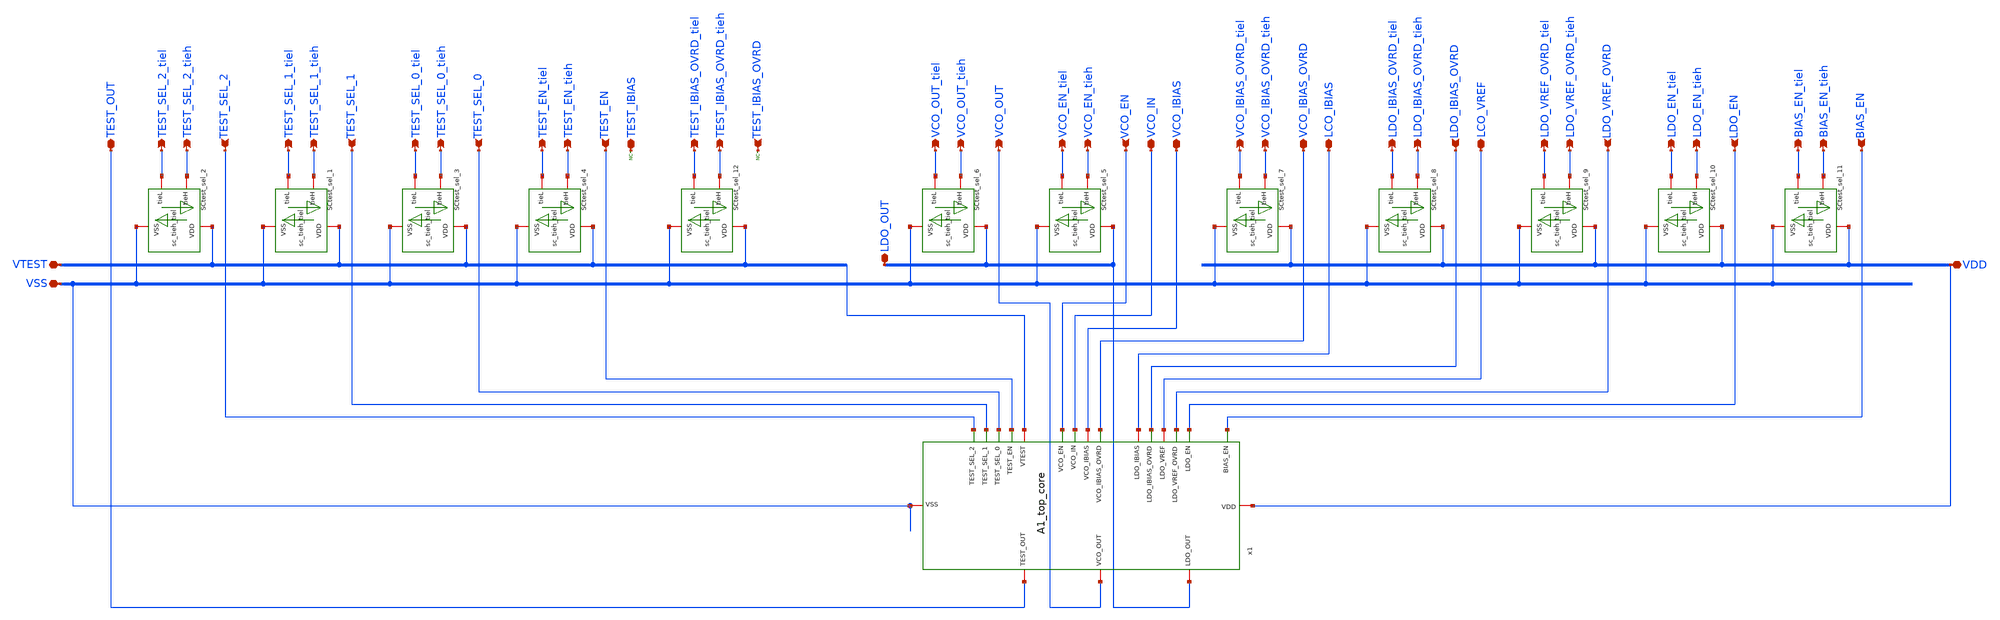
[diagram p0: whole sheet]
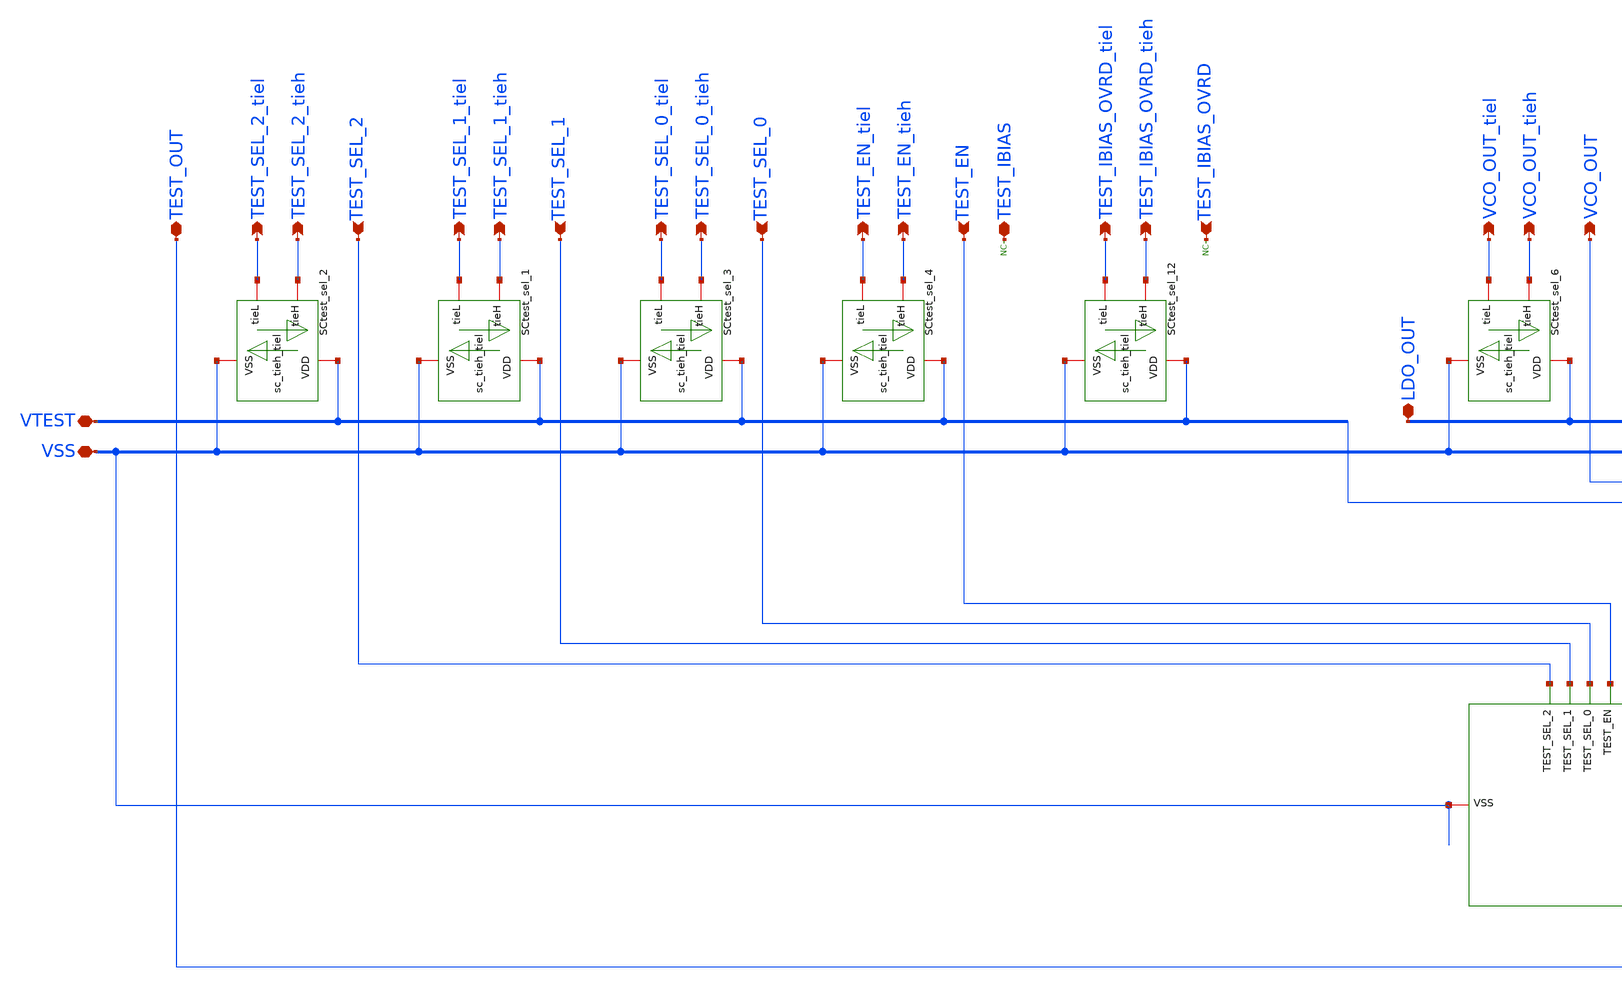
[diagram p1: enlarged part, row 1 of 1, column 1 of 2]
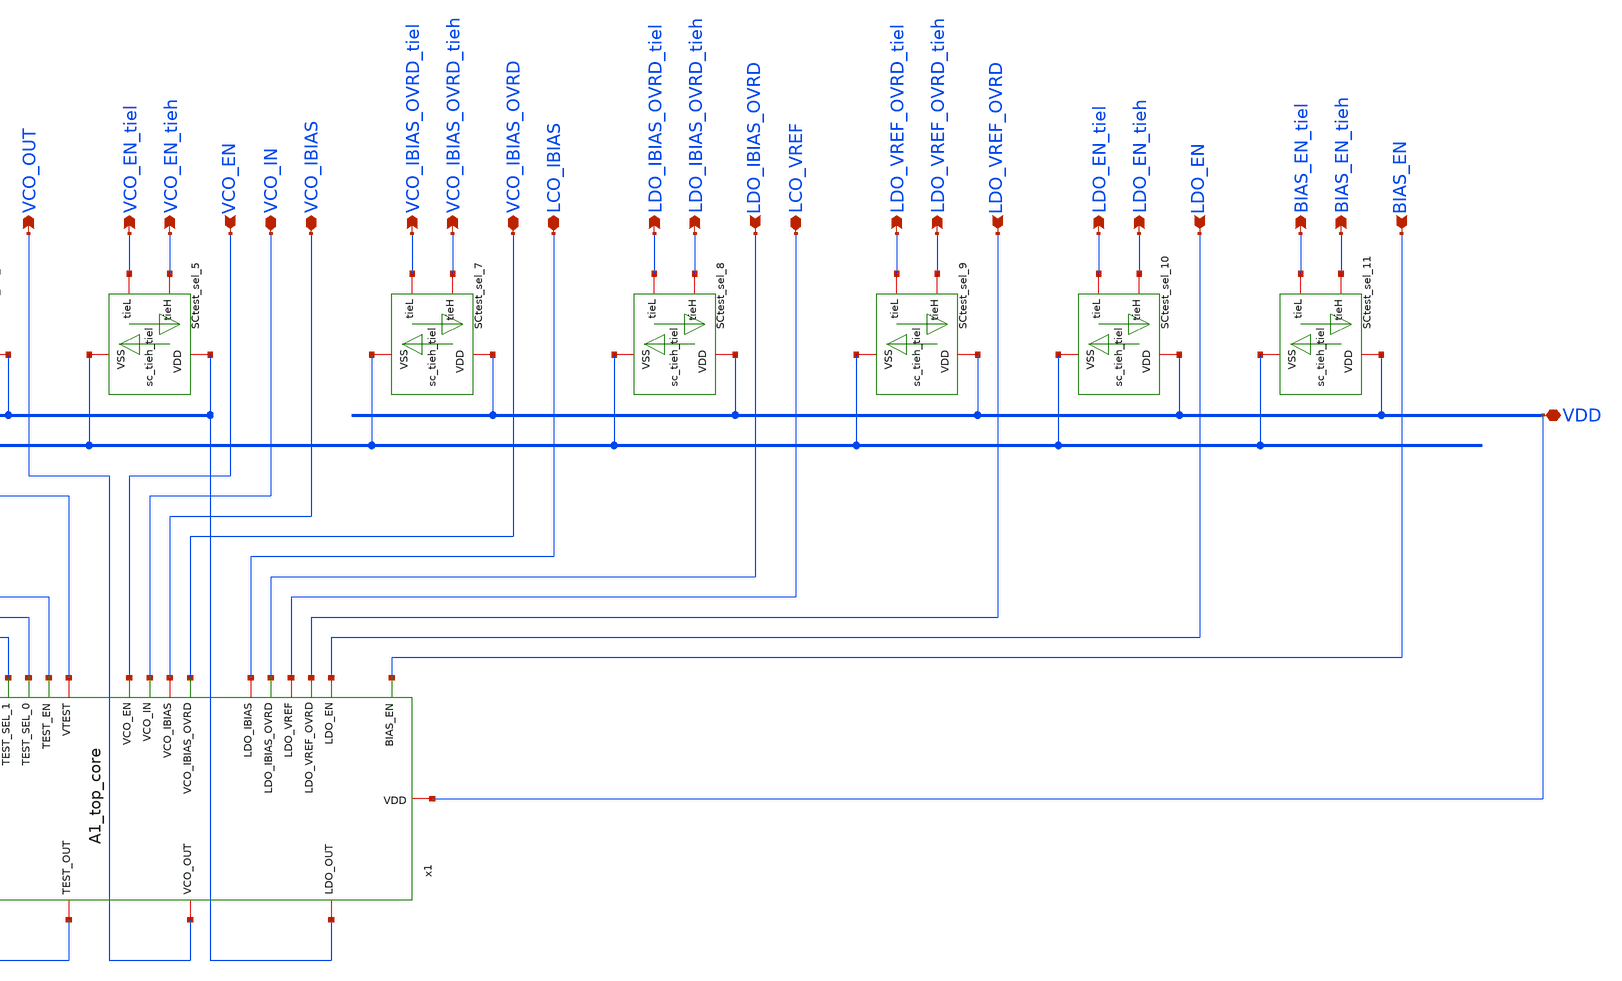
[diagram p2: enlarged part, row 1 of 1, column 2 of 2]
** sch_path: designs/libs/A1_core/A1_top/A1_top.sch
**.subckt A1_top TEST_SEL_2 TEST_SEL_2_tiel TEST_SEL_2_tieh VTEST VSS TEST_SEL_1 TEST_SEL_1_tiel
*+ TEST_SEL_1_tieh TEST_SEL_0 TEST_SEL_0_tiel TEST_SEL_0_tieh TEST_EN TEST_EN_tiel TEST_EN_tieh VCO_EN VCO_EN_tiel
*+ VCO_EN_tieh LDO_OUT VCO_OUT VCO_OUT_tiel VCO_OUT_tieh VCO_IBIAS_OVRD_tiel VCO_IBIAS_OVRD_tieh
*+ LDO_VREF_OVRD_tiel LDO_VREF_OVRD_tieh LDO_IBIAS_OVRD_tiel LDO_IBIAS_OVRD_tieh TEST_OUT VCO_IN VCO_IBIAS VCO_IBIAS_OVRD
*+ LCO_VREF LDO_VREF_OVRD LCO_IBIAS LDO_IBIAS_OVRD LDO_EN_tiel LDO_EN_tieh LDO_EN BIAS_EN_tiel BIAS_EN_tieh
*+ BIAS_EN VDD TEST_IBIAS_OVRD_tiel TEST_IBIAS_OVRD_tieh TEST_IBIAS TEST_IBIAS_OVRD
*.ipin TEST_SEL_2
*.opin TEST_SEL_2_tiel
*.opin TEST_SEL_2_tieh
*.iopin VTEST
*.iopin VSS
*.ipin TEST_SEL_1
*.opin TEST_SEL_1_tiel
*.opin TEST_SEL_1_tieh
*.ipin TEST_SEL_0
*.opin TEST_SEL_0_tiel
*.opin TEST_SEL_0_tieh
*.ipin TEST_EN
*.opin TEST_EN_tiel
*.opin TEST_EN_tieh
*.ipin VCO_EN
*.opin VCO_EN_tiel
*.opin VCO_EN_tieh
*.iopin LDO_OUT
*.opin VCO_OUT
*.opin VCO_OUT_tiel
*.opin VCO_OUT_tieh
*.opin VCO_IBIAS_OVRD_tiel
*.opin VCO_IBIAS_OVRD_tieh
*.opin LDO_VREF_OVRD_tiel
*.opin LDO_VREF_OVRD_tieh
*.opin LDO_IBIAS_OVRD_tiel
*.opin LDO_IBIAS_OVRD_tieh
*.iopin TEST_OUT
*.iopin VCO_IN
*.iopin VCO_IBIAS
*.iopin VCO_IBIAS_OVRD
*.iopin LCO_VREF
*.ipin LDO_VREF_OVRD
*.iopin LCO_IBIAS
*.ipin LDO_IBIAS_OVRD
*.opin LDO_EN_tiel
*.opin LDO_EN_tieh
*.ipin LDO_EN
*.opin BIAS_EN_tiel
*.opin BIAS_EN_tieh
*.ipin BIAS_EN
*.iopin VDD
*.opin TEST_IBIAS_OVRD_tiel
*.opin TEST_IBIAS_OVRD_tieh
*.iopin TEST_IBIAS
*.ipin TEST_IBIAS_OVRD
x1 VDD VCO_IN LDO_OUT VCO_OUT VCO_EN TEST_OUT TEST_EN TEST_SEL_0 VSS VCO_IBIAS_OVRD VCO_IBIAS LDO_EN
+ LDO_IBIAS_OVRD LCO_IBIAS LDO_VREF_OVRD LCO_VREF TEST_SEL_1 TEST_SEL_2 VTEST BIAS_EN A1_top_core
XSCtest_sel_2 TEST_SEL_2_tiel VTEST VSS TEST_SEL_2_tieh sc_tieh_tiel
XSCtest_sel_1 TEST_SEL_1_tiel VTEST VSS TEST_SEL_1_tieh sc_tieh_tiel
XSCtest_sel_3 TEST_SEL_0_tiel VTEST VSS TEST_SEL_0_tieh sc_tieh_tiel
XSCtest_sel_4 TEST_EN_tiel VTEST VSS TEST_EN_tieh sc_tieh_tiel
XSCtest_sel_5 VCO_EN_tiel LDO_OUT VSS VCO_EN_tieh sc_tieh_tiel
XSCtest_sel_6 VCO_OUT_tiel LDO_OUT VSS VCO_OUT_tieh sc_tieh_tiel
XSCtest_sel_7 VCO_IBIAS_OVRD_tiel VDD VSS VCO_IBIAS_OVRD_tieh sc_tieh_tiel
XSCtest_sel_8 LDO_IBIAS_OVRD_tiel VDD VSS LDO_IBIAS_OVRD_tieh sc_tieh_tiel
XSCtest_sel_9 LDO_VREF_OVRD_tiel VDD VSS LDO_VREF_OVRD_tieh sc_tieh_tiel
XSCtest_sel_10 LDO_EN_tiel VDD VSS LDO_EN_tieh sc_tieh_tiel
XSCtest_sel_11 BIAS_EN_tiel VDD VSS BIAS_EN_tieh sc_tieh_tiel
XSCtest_sel_12 TEST_IBIAS_OVRD_tiel VTEST VSS TEST_IBIAS_OVRD_tieh sc_tieh_tiel
* noconn TEST_IBIAS
* noconn TEST_IBIAS_OVRD
**.ends
.end
